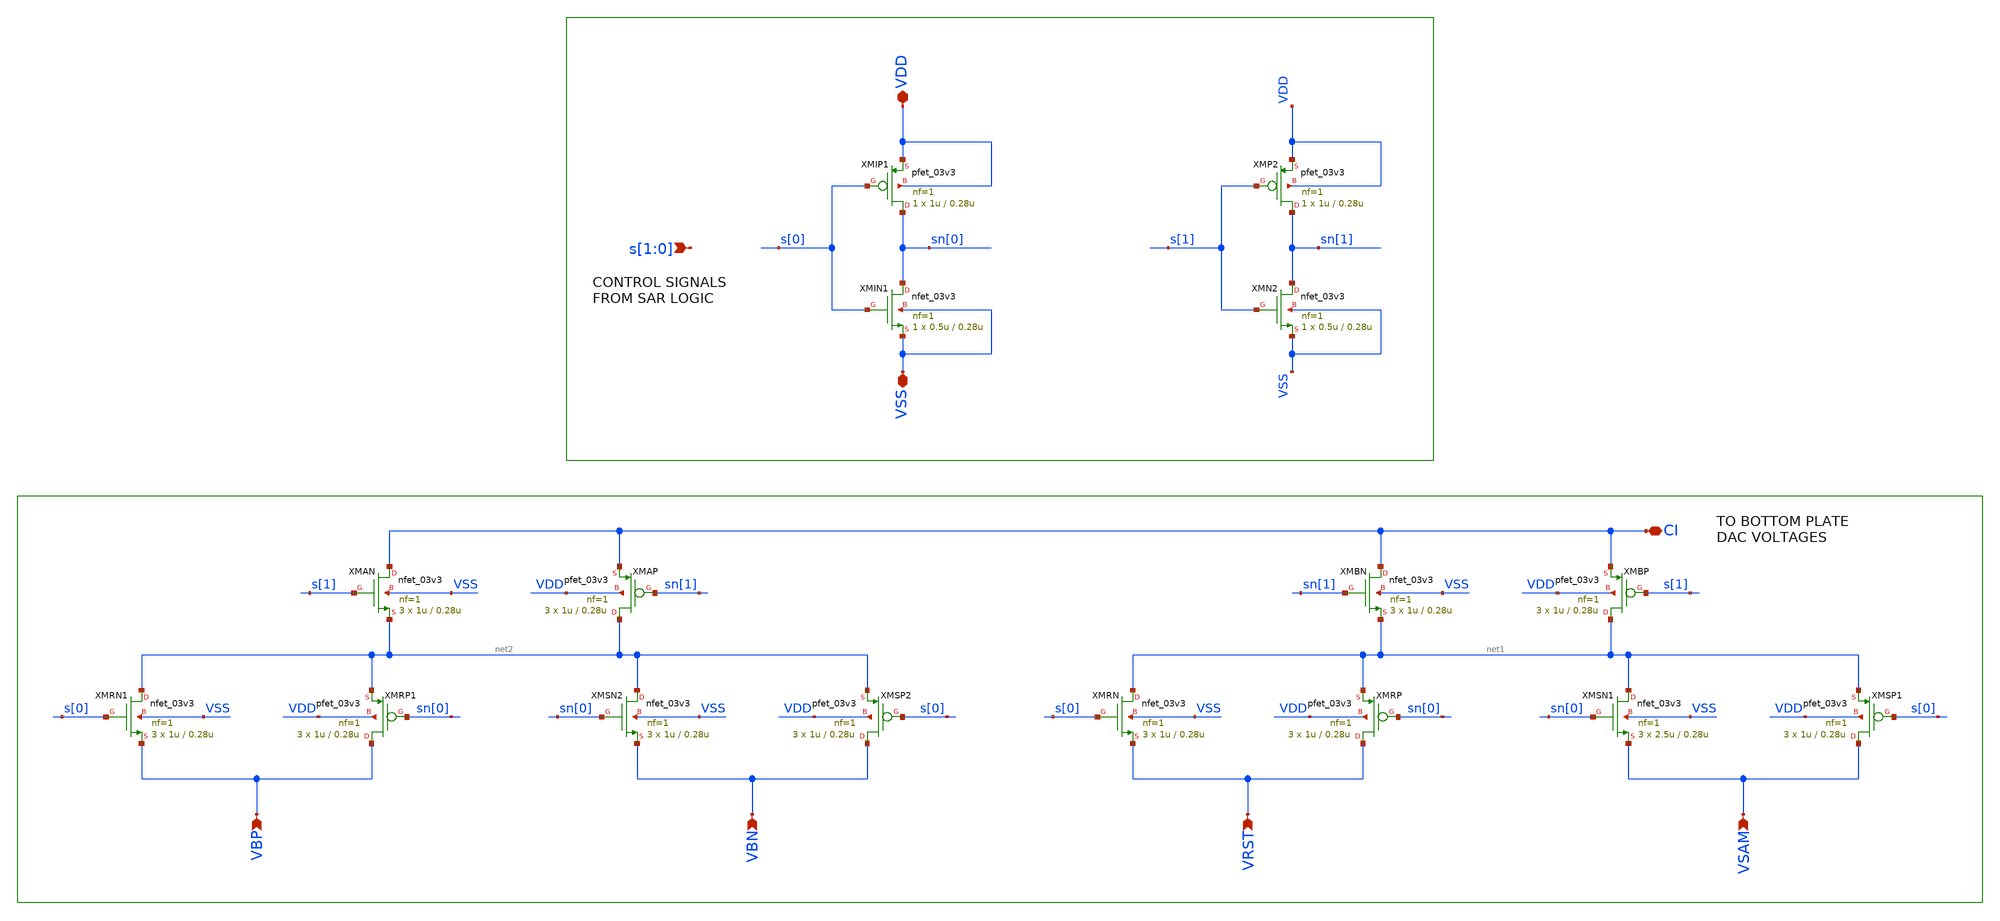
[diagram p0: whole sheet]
** sch_path: designs/sar_adc/dac/dac_sw_4state/xschem/dac_sw_4state.sch
**.subckt dac_sw_4state s[1],s[0] VDD VSS VRST CI VSAM VBP VBN
*.ipin s[1],s[0]
*.iopin VDD
*.iopin VSS
*.ipin VRST
*.iopin CI
*.ipin VSAM
*.ipin VBP
*.ipin VBN
XMIN1 sn[0] s[0] VSS VSS nfet_03v3 L=0.28u W=0.5u nf=1 ad='int((nf+1)/2) * W/nf * 0.18u' as='int((nf+2)/2) * W/nf * 0.18u'
+ pd='2*int((nf+1)/2) * (W/nf + 0.18u)' ps='2*int((nf+2)/2) * (W/nf + 0.18u)' nrd='0.18u / W' nrs='0.18u / W'
+ sa=0 sb=0 sd=0 m=1
XMIP1 sn[0] s[0] VDD VDD pfet_03v3 L=0.28u W=1u nf=1 ad='int((nf+1)/2) * W/nf * 0.18u' as='int((nf+2)/2) * W/nf * 0.18u'
+ pd='2*int((nf+1)/2) * (W/nf + 0.18u)' ps='2*int((nf+2)/2) * (W/nf + 0.18u)' nrd='0.18u / W' nrs='0.18u / W'
+ sa=0 sb=0 sd=0 m=1
XMN2 sn[1] s[1] VSS VSS nfet_03v3 L=0.28u W=0.5u nf=1 ad='int((nf+1)/2) * W/nf * 0.18u' as='int((nf+2)/2) * W/nf * 0.18u'
+ pd='2*int((nf+1)/2) * (W/nf + 0.18u)' ps='2*int((nf+2)/2) * (W/nf + 0.18u)' nrd='0.18u / W' nrs='0.18u / W'
+ sa=0 sb=0 sd=0 m=1
XMP2 sn[1] s[1] VDD VDD pfet_03v3 L=0.28u W=1u nf=1 ad='int((nf+1)/2) * W/nf * 0.18u' as='int((nf+2)/2) * W/nf * 0.18u'
+ pd='2*int((nf+1)/2) * (W/nf + 0.18u)' ps='2*int((nf+2)/2) * (W/nf + 0.18u)' nrd='0.18u / W' nrs='0.18u / W'
+ sa=0 sb=0 sd=0 m=1
XMRN net1 s[0] VRST VSS nfet_03v3 L=0.28u W=1u nf=1 ad='int((nf+1)/2) * W/nf * 0.18u' as='int((nf+2)/2) * W/nf * 0.18u'
+ pd='2*int((nf+1)/2) * (W/nf + 0.18u)' ps='2*int((nf+2)/2) * (W/nf + 0.18u)' nrd='0.18u / W' nrs='0.18u / W'
+ sa=0 sb=0 sd=0 m=3
XMRP VRST sn[0] net1 VDD pfet_03v3 L=0.28u W=1u nf=1 ad='int((nf+1)/2) * W/nf * 0.18u' as='int((nf+2)/2) * W/nf * 0.18u'
+ pd='2*int((nf+1)/2) * (W/nf + 0.18u)' ps='2*int((nf+2)/2) * (W/nf + 0.18u)' nrd='0.18u / W' nrs='0.18u / W'
+ sa=0 sb=0 sd=0 m=3
XMSN1 net1 sn[0] VSAM VSS nfet_03v3 L=0.28u W=2.5u nf=1 ad='int((nf+1)/2) * W/nf * 0.18u' as='int((nf+2)/2) * W/nf * 0.18u'
+ pd='2*int((nf+1)/2) * (W/nf + 0.18u)' ps='2*int((nf+2)/2) * (W/nf + 0.18u)' nrd='0.18u / W' nrs='0.18u / W'
+ sa=0 sb=0 sd=0 m=3
XMSP1 VSAM s[0] net1 VDD pfet_03v3 L=0.28u W=1u nf=1 ad='int((nf+1)/2) * W/nf * 0.18u' as='int((nf+2)/2) * W/nf * 0.18u'
+ pd='2*int((nf+1)/2) * (W/nf + 0.18u)' ps='2*int((nf+2)/2) * (W/nf + 0.18u)' nrd='0.18u / W' nrs='0.18u / W'
+ sa=0 sb=0 sd=0 m=3
XMBN CI sn[1] net1 VSS nfet_03v3 L=0.28u W=1u nf=1 ad='int((nf+1)/2) * W/nf * 0.18u' as='int((nf+2)/2) * W/nf * 0.18u'
+ pd='2*int((nf+1)/2) * (W/nf + 0.18u)' ps='2*int((nf+2)/2) * (W/nf + 0.18u)' nrd='0.18u / W' nrs='0.18u / W'
+ sa=0 sb=0 sd=0 m=3
XMBP net1 s[1] CI VDD pfet_03v3 L=0.28u W=1u nf=1 ad='int((nf+1)/2) * W/nf * 0.18u' as='int((nf+2)/2) * W/nf * 0.18u'
+ pd='2*int((nf+1)/2) * (W/nf + 0.18u)' ps='2*int((nf+2)/2) * (W/nf + 0.18u)' nrd='0.18u / W' nrs='0.18u / W'
+ sa=0 sb=0 sd=0 m=3
XMRN1 net2 s[0] VBP VSS nfet_03v3 L=0.28u W=1u nf=1 ad='int((nf+1)/2) * W/nf * 0.18u' as='int((nf+2)/2) * W/nf * 0.18u'
+ pd='2*int((nf+1)/2) * (W/nf + 0.18u)' ps='2*int((nf+2)/2) * (W/nf + 0.18u)' nrd='0.18u / W' nrs='0.18u / W'
+ sa=0 sb=0 sd=0 m=3
XMRP1 VBP sn[0] net2 VDD pfet_03v3 L=0.28u W=1u nf=1 ad='int((nf+1)/2) * W/nf * 0.18u' as='int((nf+2)/2) * W/nf * 0.18u'
+ pd='2*int((nf+1)/2) * (W/nf + 0.18u)' ps='2*int((nf+2)/2) * (W/nf + 0.18u)' nrd='0.18u / W' nrs='0.18u / W'
+ sa=0 sb=0 sd=0 m=3
XMSN2 net2 sn[0] VBN VSS nfet_03v3 L=0.28u W=1u nf=1 ad='int((nf+1)/2) * W/nf * 0.18u' as='int((nf+2)/2) * W/nf * 0.18u'
+ pd='2*int((nf+1)/2) * (W/nf + 0.18u)' ps='2*int((nf+2)/2) * (W/nf + 0.18u)' nrd='0.18u / W' nrs='0.18u / W'
+ sa=0 sb=0 sd=0 m=3
XMSP2 VBN s[0] net2 VDD pfet_03v3 L=0.28u W=1u nf=1 ad='int((nf+1)/2) * W/nf * 0.18u' as='int((nf+2)/2) * W/nf * 0.18u'
+ pd='2*int((nf+1)/2) * (W/nf + 0.18u)' ps='2*int((nf+2)/2) * (W/nf + 0.18u)' nrd='0.18u / W' nrs='0.18u / W'
+ sa=0 sb=0 sd=0 m=3
XMAN CI s[1] net2 VSS nfet_03v3 L=0.28u W=1u nf=1 ad='int((nf+1)/2) * W/nf * 0.18u' as='int((nf+2)/2) * W/nf * 0.18u'
+ pd='2*int((nf+1)/2) * (W/nf + 0.18u)' ps='2*int((nf+2)/2) * (W/nf + 0.18u)' nrd='0.18u / W' nrs='0.18u / W'
+ sa=0 sb=0 sd=0 m=3
XMAP net2 sn[1] CI VDD pfet_03v3 L=0.28u W=1u nf=1 ad='int((nf+1)/2) * W/nf * 0.18u' as='int((nf+2)/2) * W/nf * 0.18u'
+ pd='2*int((nf+1)/2) * (W/nf + 0.18u)' ps='2*int((nf+2)/2) * (W/nf + 0.18u)' nrd='0.18u / W' nrs='0.18u / W'
+ sa=0 sb=0 sd=0 m=3
**.ends
.end
